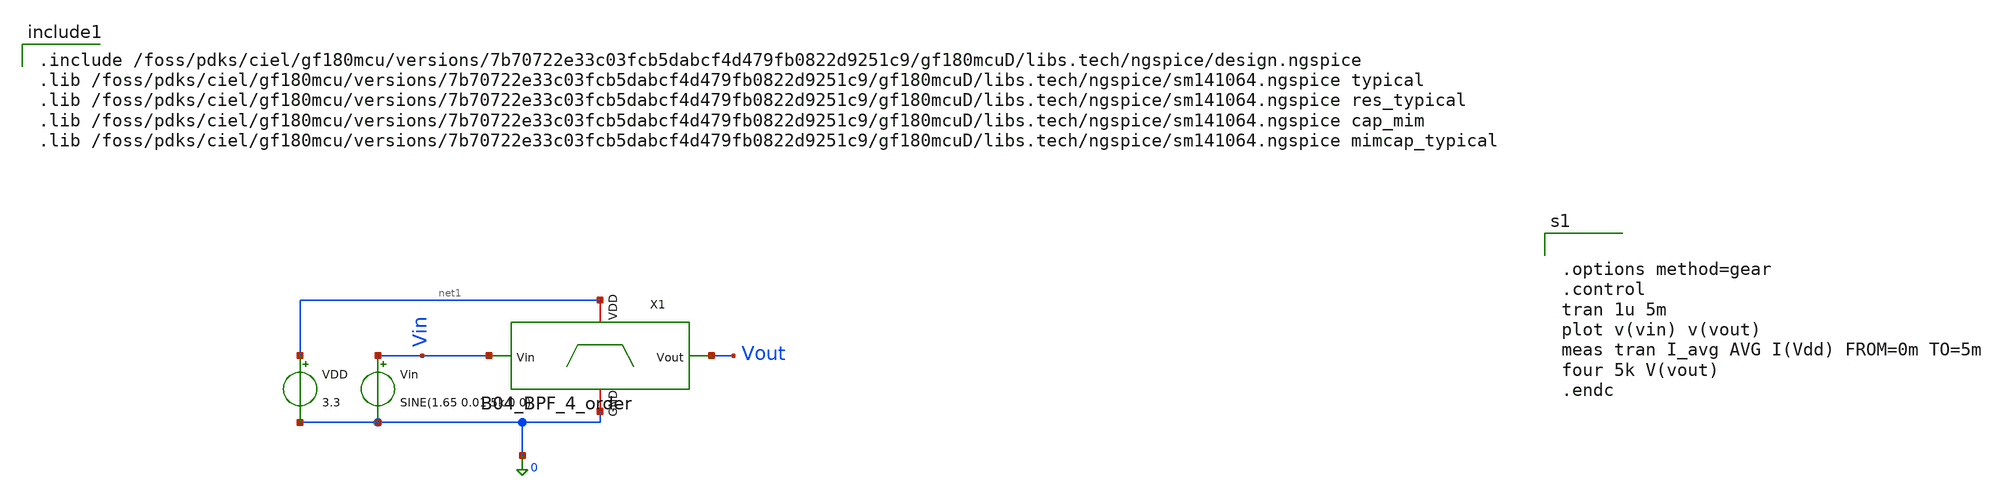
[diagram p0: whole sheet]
** sch_path: analog/B04_tb_BPF_4_order_tran.sch
**.subckt B04_tb_BPF_4_order_tran
Vin Vin 0 SINE(1.65 0.01 5k 0 0)
VDD net1 0 3.3
X1 net1 Vout Vin 0 B04_BPF_4_order
**** begin user architecture code

.include /foss/pdks/ciel/gf180mcu/versions/7b70722e33c03fcb5dabcf4d479fb0822d9251c9/gf180mcuD/libs.tech/ngspice/design.ngspice
.lib /foss/pdks/ciel/gf180mcu/versions/7b70722e33c03fcb5dabcf4d479fb0822d9251c9/gf180mcuD/libs.tech/ngspice/sm141064.ngspice typical
.lib /foss/pdks/ciel/gf180mcu/versions/7b70722e33c03fcb5dabcf4d479fb0822d9251c9/gf180mcuD/libs.tech/ngspice/sm141064.ngspice res_typical
.lib /foss/pdks/ciel/gf180mcu/versions/7b70722e33c03fcb5dabcf4d479fb0822d9251c9/gf180mcuD/libs.tech/ngspice/sm141064.ngspice cap_mim
.lib /foss/pdks/ciel/gf180mcu/versions/7b70722e33c03fcb5dabcf4d479fb0822d9251c9/gf180mcuD/libs.tech/ngspice/sm141064.ngspice mimcap_typical



.options method=gear
.control
tran 1u 5m
plot v(vin) v(vout)
meas tran I_avg AVG I(Vdd) FROM=0m TO=5m
four 5k V(vout)
.endc


**** end user architecture code
**.ends
.end
